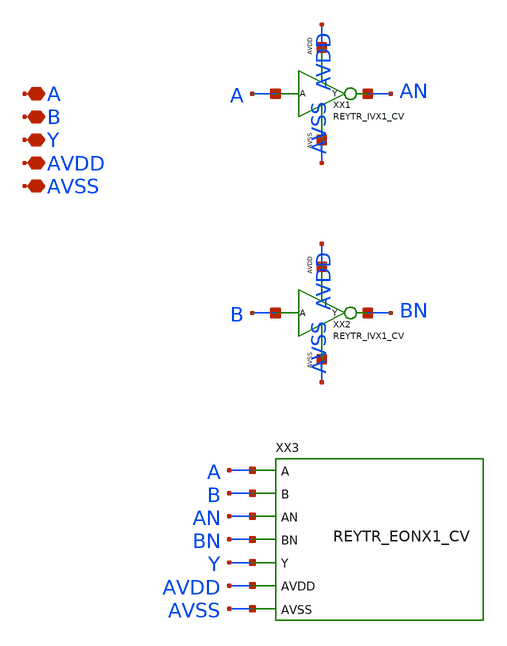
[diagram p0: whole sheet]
** sch_path: design/REY_TR_SKY130A/REYTR_EOX1_CV.sch
**.subckt REYTR_EOX1_CV A B Y AVDD AVSS
*.iopin A
*.iopin B
*.iopin Y
*.iopin AVDD
*.iopin AVSS
XX1 A AN AVDD AVSS REYTR_IVX1_CV
XX2 B BN AVDD AVSS REYTR_IVX1_CV
XX3 A B AN BN Y AVDD AVSS REYTR_EONX1_CV
**.ends
.end
